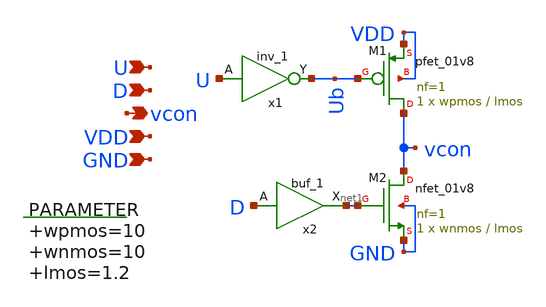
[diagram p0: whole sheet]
** sch_path: xschem/charge_pump.sch
**.subckt charge_pump U D vcon VDD GND
*.ipin U
*.ipin D
*.opin vcon
*.ipin VDD
*.ipin GND
XM1 vcon Ub VDD VDD sky130_fd_pr__pfet_01v8 L=lmos W=wpmos nf=1 ad='int((nf+1)/2) * W/nf * 0.29' as='int((nf+2)/2) * W/nf * 0.29'
+ pd='2*int((nf+1)/2) * (W/nf + 0.29)' ps='2*int((nf+2)/2) * (W/nf + 0.29)' nrd='0.29 / W' nrs='0.29 / W'
+ sa=0 sb=0 sd=0 mult=1 m=1
XM2 vcon net1 GND GND sky130_fd_pr__nfet_01v8 L=lmos W=wnmos nf=1 ad='int((nf+1)/2) * W/nf * 0.29' as='int((nf+2)/2) * W/nf * 0.29'
+ pd='2*int((nf+1)/2) * (W/nf + 0.29)' ps='2*int((nf+2)/2) * (W/nf + 0.29)' nrd='0.29 / W' nrs='0.29 / W'
+ sa=0 sb=0 sd=0 mult=1 m=1
x1 U GND GND VDD VDD Ub sky130_fd_sc_hd__inv_1
.param wpmos=10 wnmos=10 lmos=1.2
x2 D GND GND VDD VDD net1 sky130_fd_sc_hd__buf_1
**.ends
.end
